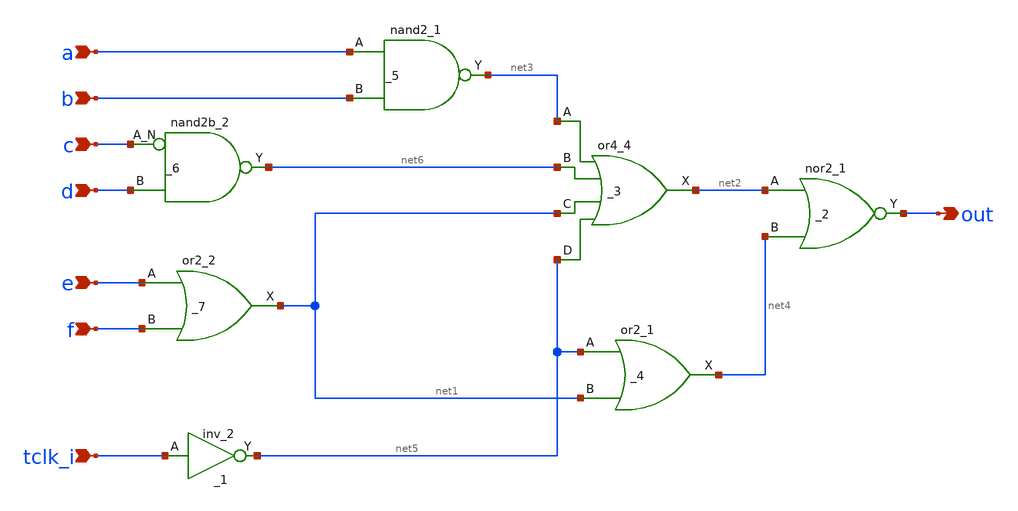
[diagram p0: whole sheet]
** sch_path: test_directory/bck/rn_wrapper.sch
**.subckt rn_wrapper tclk_i a b c d e f out
*.ipin tclk_i
*.ipin a
*.ipin b
*.ipin c
*.ipin d
*.ipin e
*.ipin f
*.opin out
_1 tclk_i VGND VNB VPB VPWR net5 sky130_fd_sc_hd__inv_2
_2 net2 net4 VGND VNB VPB VPWR out sky130_fd_sc_hd__nor2_1
_3 net3 net6 net1 net5 VGND VNB VPB VPWR net2 sky130_fd_sc_hd__or4_4
_4 net5 net1 VGND VNB VPB VPWR net4 sky130_fd_sc_hd__or2_1
_5 a b VGND VNB VPB VPWR net3 sky130_fd_sc_hd__nand2_1
_6 c d VGND VNB VPB VPWR net6 sky130_fd_sc_hd__nand2b_2
_7 e f VGND VNB VPB VPWR net1 sky130_fd_sc_hd__or2_2
**.ends
.end
